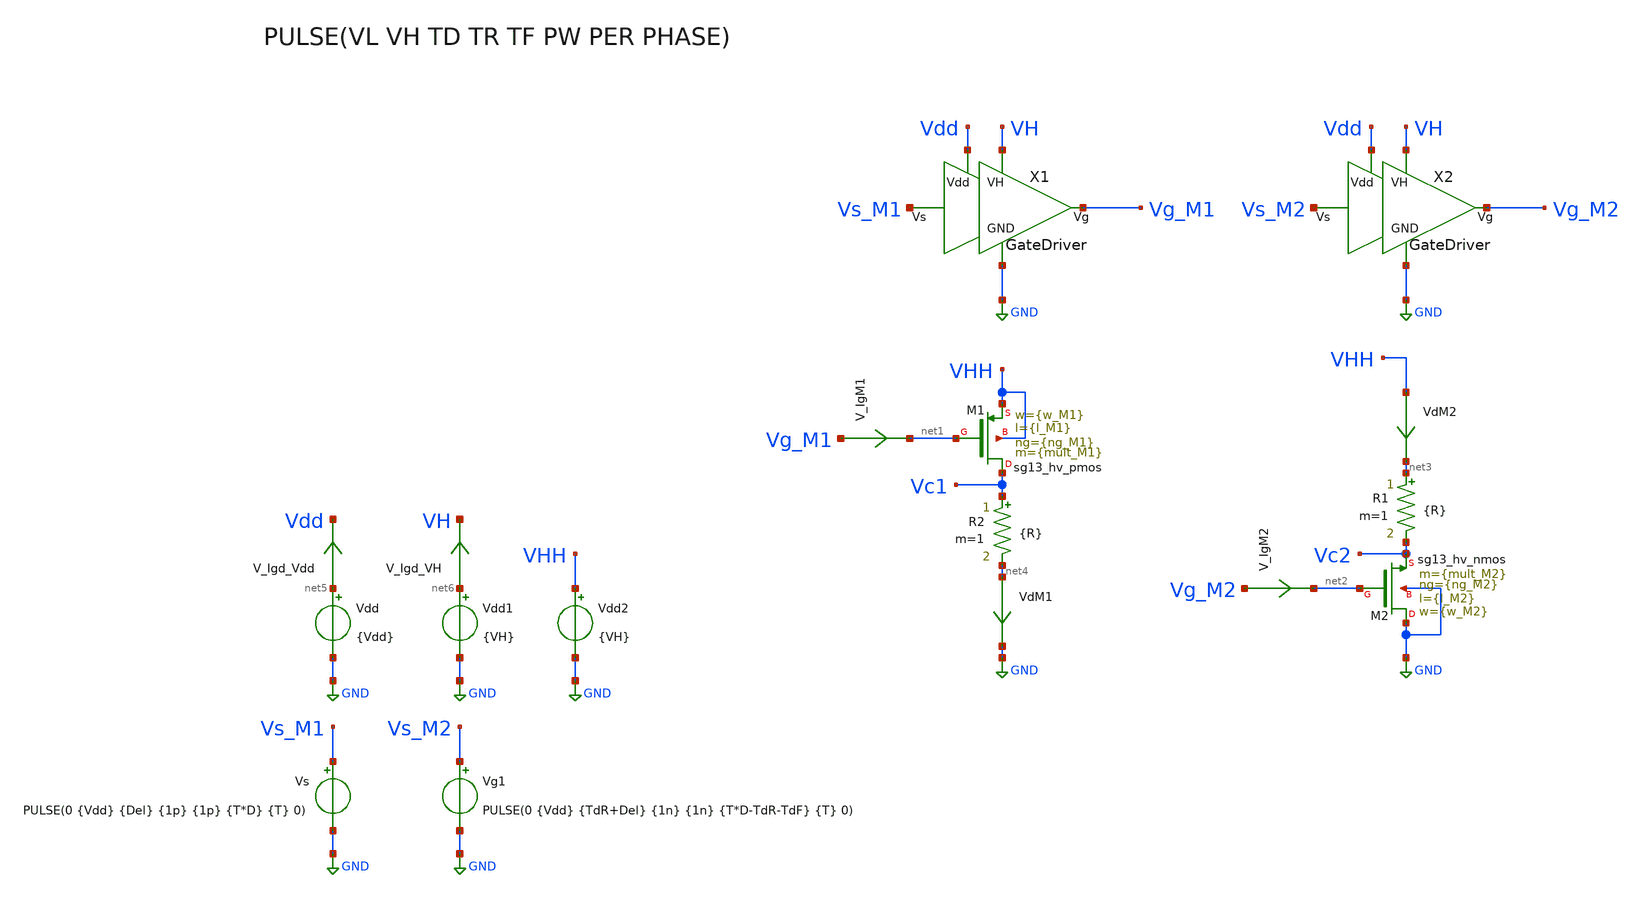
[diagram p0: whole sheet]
** sch_path: ChipUSM_AnalogTrack24/GD/TB_GateDriver_hvMOS.sch
**.subckt TB_GateDriver_hvMOS
X1 Vs_M1 Vg_M1 Vdd VH GND GateDriver
Vdd net5 GND {Vdd}
Vs Vs_M1 GND PULSE(0 {Vdd} {Del} {1p} {1p} {T*D} {T} 0)
Vdd1 net6 GND {VH}
XM2 GND net2 Vc2 GND sg13_hv_nmos w={w_M2} l={l_M2} ng={ng_M2} m={mult_M2} mm_ok=1
XM1 Vc1 net1 VHH VHH sg13_hv_pmos w={w_M1} l={l_M1} ng={ng_M1} m={mult_M1} mm_ok=1
VdM2 VHH net3 0
.save i(vdm2)
VdM1 net4 GND 0
.save i(vdm1)
Vg1 Vs_M2 GND PULSE(0 {Vdd} {TdR+Del} {1n} {1n} {T*D-TdR-TdF} {T} 0)
R1 net3 Vc2 {R} m=1
R2 Vc1 net4 {R} m=1
X2 Vs_M2 Vg_M2 Vdd VH GND GateDriver
V_IgM1 Vg_M1 net1 0
.save i(v_igm1)
V_IgM2 Vg_M2 net2 0
.save i(v_igm2)
Vdd2 VHH GND {VH}
V_Igd_Vdd net5 Vdd 0
.save i(v_igd_vdd)
V_Igd_VH net6 VH 0
.save i(v_igd_vh)
**** begin user architecture code

.lib cornerMOShv.lib mos_tt
.lib cornerMOSlv.lib mos_tt



.param Vdd = 1.2
.param VH = 3.3

*.param T = 1u
*.param TdR = 0.1u
*.param TdF = 0.1u

.param D = 0.5
.param T = 0.1u
.param TdR = 1n
.param TdF = 1n
.param TR = 10n
.param TF = 10n
.param Del = 0.05u

.param R = 3.3

.param temp = 27






.save all
.control
reset
set color0 = white
tran 1n 1u

let VsdM1 = v(VH) - v(Vc1)
let VdsM2 = v(Vc2)
let P_GD_Vdd = i(V_Igd_Vdd)*v(Vdd)
let P_GD_VH = i(V_Igd_VH)*v(VH)

plot i(VdM1) i(VdM2)
plot v(Vc1) v(Vc2)
plot v(Vg_M1) v(Vg_M2)
plot VsdM1 VdsM2
plot v(Vs_M1) v(Vs_M2)
*plot v(x1.VgMD2)
*plot v(x1.VgMD5)
*plot v(x1.VgMD78)

plot i(V_IgM1) i(V_IgM2)
plot i(x1.VIg78)
*plot v(x2.VgMD2)
*plot v(x2.VgMD5)
*plot v(x2.VgMD78)

meas tran P_GD_Vdd_mean AVG P_GD_Vdd from=0.5u to=1u
meas tran P_GD_VH_mean AVG P_GD_VH from=0.5u to=1u

let P_GD = P_GD_Vdd_mean + P_GD_VH_mean

meas TRAN td_off_M1 TRIG v(Vg_M1) VAL=0.33 RISE=1 TARG VsdM1 VAL=0.33 RISE=1
meas TRAN td_on_M1 TRIG v(Vg_M1) VAL=2.97 FALL=1 TARG VsdM1 VAL=2.97 FALL=1
meas TRAN td_on_M2 TRIG v(Vg_M2) VAL=0.33 RISE=1 TARG VdsM2 VAL=2.97 FALL=1
meas TRAN td_off_M2 TRIG v(Vg_M2) VAL=2.97 FALL=1 TARG VdsM2 VAL=0.33 RISE=1

meas TRAN tPdR1 TRIG v(Vs_M1) VAL=0.12 RISE=1 TARG v(Vg_M1) VAL=0.33 RISE=1
meas TRAN tPdF1 TRIG v(Vs_M1) VAL=1.08 FALL=1 TARG v(Vg_M1) VAL=2.97 FALL=1
*meas TRAN tPdR1 TRIG v(Vg_M2) VAL=2.97 FALL=1 TARG VdsM2 VAL=0.33 RISE=1
*meas TRAN tPdR1 TRIG v(Vg_M2) VAL=2.97 FALL=1 TARG VdsM2 VAL=0.33 RISE=1
let TdR = td_off_M1 - td_on_M2
let TdF = td_on_M1 - td_off_M2
print TdR TdF P_GD


.endc

.end




.param temp=27

*.param mult_13 = 1
*.param mult_24 = 6
*.param mult_5 = 100
*.param mult_6 = 100
*.param mult_7 = 200
*.param mult_8 = 200
*.param mult_9 = 5
*.param mult_10 = 5

.param mult_13 = 1
.param mult_24 = 6
.param mult_5 = 30
.param mult_6 = 25
.param mult_7 = 250
.param mult_8 = 200
.param mult_9 = 15
.param mult_10 = 15
*.param mult_5 = 25
*.param mult_6 = 25
*.param mult_7 = 75
*.param mult_8 = 60

.param ng_13 = 1
.param ng_24 = 1
.param ng_5 = 1
.param ng_6 = 1
.param ng_7 = 1
.param ng_8 = 1
.param ng_9 = 1
.param ng_10 = 1

*.param w_1357 = 0.3u
*.param w_2468 = 0.3u

.param l_1357 = 0.4u
.param w_1357 = 10u
.param l_2468 = 0.45u
.param w_2468 = 10u
.param l_9 = 0.13u
.param w_9 = 0.15u
.param l_10 = 0.13u
.param w_10 = 0.15u






.param temp=27
.param mult_M1 = 12000
.param w_M1 =10u
.param l_M1 = 0.4u
.param ng_M1 = 1

.param mult_M2 = 4000
.param w_M2 =10u
.param l_M2 =0.45u
.param ng_M2 =1





**** end user architecture code
**.ends

* expanding   symbol:  GateDriver.sym # of pins=5
** sym_path: ChipUSM_AnalogTrack24/GD/GateDriver.sym
** sch_path: ChipUSM_AnalogTrack24/GD/GateDriver.sch
.subckt GateDriver Vs Vg Vdd VH GND
*.iopin VH
*.iopin Vdd
*.ipin Vs
*.opin Vg
*.iopin GND
XMD9 VgMD2 Vs Vdd Vdd sg13_lv_pmos w={w_9} l={l_9} ng={ng_9} m={mult_9} mm_ok=1
XMD10 GND Vs VgMD2 GND sg13_lv_nmos w={w_10} l={l_10} ng={ng_10} m={mult_10} mm_ok=1
XMD1 VgMD5 net1 VH VH sg13_hv_pmos w={w_1357} l={l_1357} ng={ng_13} m={mult_13} mm_ok=1
XMD3 net1 VgMD5 VH VH sg13_hv_pmos w={w_1357} l={l_1357} ng={ng_13} m={mult_13} mm_ok=1
XMD5 net2 VgMD5 VH VH sg13_hv_pmos w={w_1357} l={l_1357} ng={ng_5} m={mult_5} mm_ok=1
XMD7 Vg VgMd78 VH VH sg13_hv_pmos w={w_1357} l={l_1357} ng={ng_7} m={mult_7} mm_ok=1
XMD2 GND VgMD2 VgMD5 GND sg13_hv_nmos w={w_2468} l={l_2468} ng={ng_24} m={mult_24} mm_ok=1
XMD4 GND Vs net1 GND sg13_hv_nmos w={w_2468} l={l_2468} ng={ng_24} m={mult_24} mm_ok=1
XMD6 GND Vs net2 GND sg13_hv_nmos w={w_2468} l={l_2468} ng={ng_6} m={mult_6} mm_ok=1
XMD8 GND VgMd78 Vg GND sg13_hv_nmos w={w_2468} l={l_2468} ng={ng_8} m={mult_8} mm_ok=1
VIg78 net2 VgMd78 0
.save i(vig78)
.ends

.GLOBAL GND
.end
